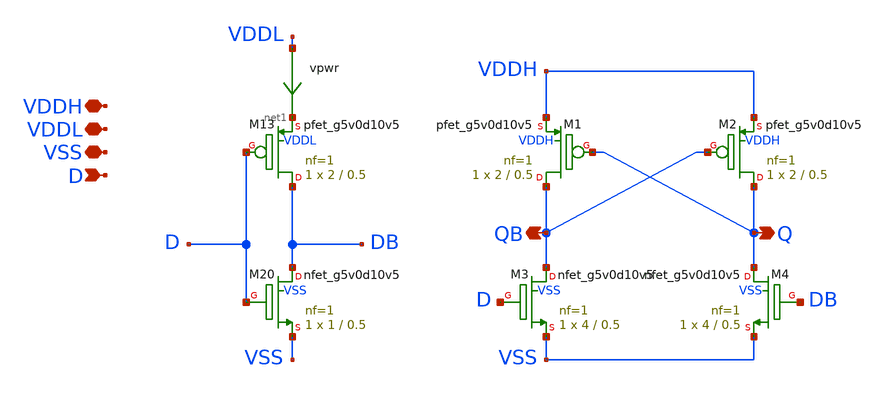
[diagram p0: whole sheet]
** sch_path: xschem/lvl_shift_lohi1.sch
**.subckt lvl_shift_lohi1 Q D VDDH VDDL VSS QB
*.opin Q
*.ipin D
*.iopin VDDH
*.iopin VDDL
*.iopin VSS
*.opin QB
vpwr VDDL net1 0
.save i(vpwr)
XM13 DB D net1 VDDL sky130_fd_pr__pfet_g5v0d10v5 L=0.5 W=2 nf=1 ad='int((nf+1)/2) * W/nf * 0.29' as='int((nf+2)/2) * W/nf * 0.29'
+ pd='2*int((nf+1)/2) * (W/nf + 0.29)' ps='2*int((nf+2)/2) * (W/nf + 0.29)' nrd='0.29 / W' nrs='0.29 / W'
+ sa=0 sb=0 sd=0 mult=1 m=1
XM20 DB D VSS VSS sky130_fd_pr__nfet_g5v0d10v5 L=0.5 W=1 nf=1 ad='int((nf+1)/2) * W/nf * 0.29' as='int((nf+2)/2) * W/nf * 0.29'
+ pd='2*int((nf+1)/2) * (W/nf + 0.29)' ps='2*int((nf+2)/2) * (W/nf + 0.29)' nrd='0.29 / W' nrs='0.29 / W'
+ sa=0 sb=0 sd=0 mult=1 m=1
XM1 QB Q VDDH VDDH sky130_fd_pr__pfet_g5v0d10v5 L=0.5 W=2 nf=1 ad='int((nf+1)/2) * W/nf * 0.29' as='int((nf+2)/2) * W/nf * 0.29'
+ pd='2*int((nf+1)/2) * (W/nf + 0.29)' ps='2*int((nf+2)/2) * (W/nf + 0.29)' nrd='0.29 / W' nrs='0.29 / W'
+ sa=0 sb=0 sd=0 mult=1 m=1
XM2 Q QB VDDH VDDH sky130_fd_pr__pfet_g5v0d10v5 L=0.5 W=2 nf=1 ad='int((nf+1)/2) * W/nf * 0.29' as='int((nf+2)/2) * W/nf * 0.29'
+ pd='2*int((nf+1)/2) * (W/nf + 0.29)' ps='2*int((nf+2)/2) * (W/nf + 0.29)' nrd='0.29 / W' nrs='0.29 / W'
+ sa=0 sb=0 sd=0 mult=1 m=1
XM3 QB D VSS VSS sky130_fd_pr__nfet_g5v0d10v5 L=0.5 W=4 nf=1 ad='int((nf+1)/2) * W/nf * 0.29' as='int((nf+2)/2) * W/nf * 0.29'
+ pd='2*int((nf+1)/2) * (W/nf + 0.29)' ps='2*int((nf+2)/2) * (W/nf + 0.29)' nrd='0.29 / W' nrs='0.29 / W'
+ sa=0 sb=0 sd=0 mult=1 m=1
XM4 Q DB VSS VSS sky130_fd_pr__nfet_g5v0d10v5 L=0.5 W=4 nf=1 ad='int((nf+1)/2) * W/nf * 0.29' as='int((nf+2)/2) * W/nf * 0.29'
+ pd='2*int((nf+1)/2) * (W/nf + 0.29)' ps='2*int((nf+2)/2) * (W/nf + 0.29)' nrd='0.29 / W' nrs='0.29 / W'
+ sa=0 sb=0 sd=0 mult=1 m=1
**.ends
.end
